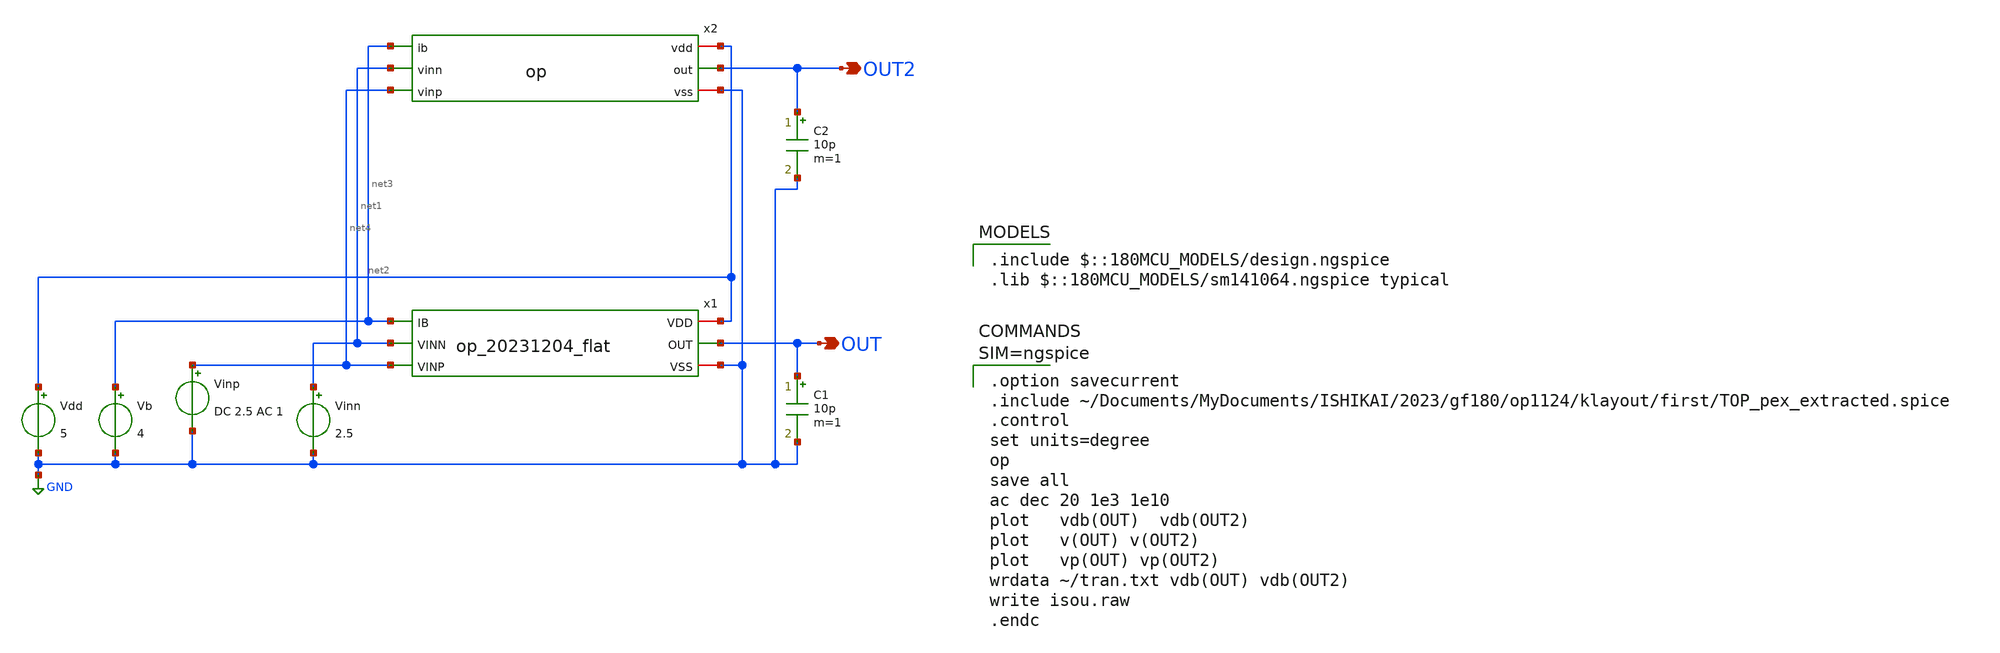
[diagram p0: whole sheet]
** sch_path: member_project/gitefu/op_tb.sch
**.subckt op_tb OUT2 OUT
*.opin OUT2
*.opin OUT
Vdd net2 GND 5
Vinp net4 GND DC 2.5 AC 1
Vinn net1 GND 2.5
C2 OUT2 GND 10p m=1
x2
Vb net3 GND 4
C1 OUT GND 10p m=1
x1 GND OUT net4 net2 net1 net3 TOP
**** begin user architecture code
 .include $::180MCU_MODELS/design.ngspice
.lib $::180MCU_MODELS/sm141064.ngspice typical


.option savecurrent
.include ~/Documents/MyDocuments/ISHIKAI/2023/gf180/op1124/klayout/first/TOP_pex_extracted.spice
.control
set units=degree
op
save all
ac dec 20 1e3 1e10
plot   vdb(OUT)  vdb(OUT2)
plot   v(OUT) v(OUT2)
plot   vp(OUT) vp(OUT2)
wrdata ~/tran.txt vdb(OUT) vdb(OUT2)
write isou.raw
.endc



**** end user architecture code
**.ends
.GLOBAL GND
.end
